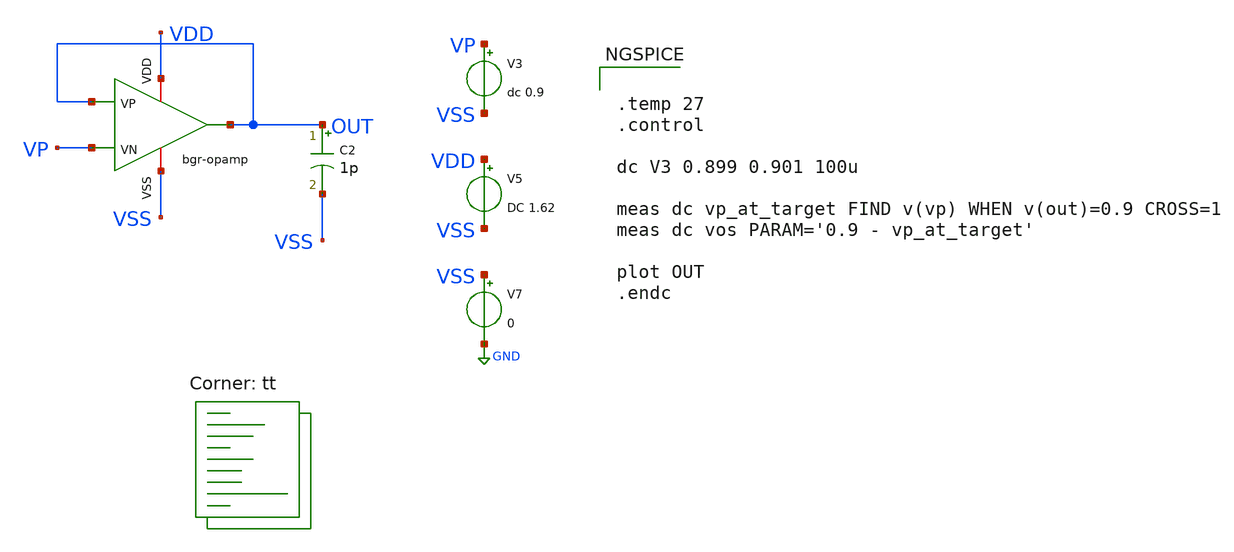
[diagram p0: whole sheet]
** sch_path: bandgap/bgr-opamp/tb_dc.sch
**.subckt tb_dc
V3 VP VSS dc 0.9
V5 VDD VSS DC 1.62
V7 VSS GND 0
C2 OUT VSS 1p m=1
x1 VDD OUT OUT VP VSS bgr-opamp
**** begin user architecture code


.temp 27
.control

dc V3 0.899 0.901 100u

meas dc vp_at_target FIND v(vp) WHEN v(out)=0.9 CROSS=1
meas dc vos PARAM='0.9 - vp_at_target'

plot OUT
.endc


.lib $::SKYWATER_MODELS/sky130.lib.spice tt
**** end user architecture code
**.ends

* expanding   symbol:  afe-icdec-teknofest-2026/bandgap/bgr-opamp/bgr-opamp.sym # of pins=5
** sym_path: bandgap/bgr-opamp/bgr-opamp.sym
** sch_path: bandgap/bgr-opamp/bgr-opamp.sch
.subckt bgr-opamp VDD OUT VP VN VSS
*.iopin VSS
*.iopin VDD
*.ipin VP
*.ipin VN
*.opin OUT
XM2 net2 VN net3 VSS sky130_fd_pr__nfet_01v8 L=0.3 W=30 nf=2 ad='int((nf+1)/2) * W/nf * 0.29' as='int((nf+2)/2) * W/nf * 0.29'
+ pd='2*int((nf+1)/2) * (W/nf + 0.29)' ps='2*int((nf+2)/2) * (W/nf + 0.29)' nrd='0.29 / W' nrs='0.29 / W'
+ sa=0 sb=0 sd=0 mult=1 m=1
XM4 net2 net1 VDD VDD sky130_fd_pr__pfet_01v8 L=1.25 W=10.8 nf=4 ad='int((nf+1)/2) * W/nf * 0.29' as='int((nf+2)/2) * W/nf * 0.29'
+ pd='2*int((nf+1)/2) * (W/nf + 0.29)' ps='2*int((nf+2)/2) * (W/nf + 0.29)' nrd='0.29 / W' nrs='0.29 / W'
+ sa=0 sb=0 sd=0 mult=1 m=1
XM3 net1 net1 VDD VDD sky130_fd_pr__pfet_01v8 L=1.25 W=10.8 nf=4 ad='int((nf+1)/2) * W/nf * 0.29' as='int((nf+2)/2) * W/nf * 0.29'
+ pd='2*int((nf+1)/2) * (W/nf + 0.29)' ps='2*int((nf+2)/2) * (W/nf + 0.29)' nrd='0.29 / W' nrs='0.29 / W'
+ sa=0 sb=0 sd=0 mult=1 m=1
XM5 net3 net11 VSS VSS sky130_fd_pr__nfet_01v8 L=1.25 W=3.4 nf=1 ad='int((nf+1)/2) * W/nf * 0.29' as='int((nf+2)/2) * W/nf * 0.29'
+ pd='2*int((nf+1)/2) * (W/nf + 0.29)' ps='2*int((nf+2)/2) * (W/nf + 0.29)' nrd='0.29 / W' nrs='0.29 / W'
+ sa=0 sb=0 sd=0 mult=1 m=1
XM9 net4 net5 net12 VSS sky130_fd_pr__nfet_01v8 L=1.25 W=13.6 nf=1 ad='int((nf+1)/2) * W/nf * 0.29' as='int((nf+2)/2) * W/nf * 0.29'
+ pd='2*int((nf+1)/2) * (W/nf + 0.29)' ps='2*int((nf+2)/2) * (W/nf + 0.29)' nrd='0.29 / W' nrs='0.29 / W'
+ sa=0 sb=0 sd=0 mult=1 m=1
XM8 net4 net4 VDD VDD sky130_fd_pr__pfet_01v8 L=1.25 W=10.8 nf=4 ad='int((nf+1)/2) * W/nf * 0.29' as='int((nf+2)/2) * W/nf * 0.29'
+ pd='2*int((nf+1)/2) * (W/nf + 0.29)' ps='2*int((nf+2)/2) * (W/nf + 0.29)' nrd='0.29 / W' nrs='0.29 / W'
+ sa=0 sb=0 sd=0 mult=1 m=1
XM11 net5 net4 VDD VDD sky130_fd_pr__pfet_01v8 L=1.25 W=10.8 nf=4 ad='int((nf+1)/2) * W/nf * 0.29' as='int((nf+2)/2) * W/nf * 0.29'
+ pd='2*int((nf+1)/2) * (W/nf + 0.29)' ps='2*int((nf+2)/2) * (W/nf + 0.29)' nrd='0.29 / W' nrs='0.29 / W'
+ sa=0 sb=0 sd=0 mult=1 m=1
XM10 net5 net5 net6 net6 sky130_fd_pr__nfet_01v8 L=1.25 W=3.4 nf=1 ad='int((nf+1)/2) * W/nf * 0.29' as='int((nf+2)/2) * W/nf * 0.29'
+ pd='2*int((nf+1)/2) * (W/nf + 0.29)' ps='2*int((nf+2)/2) * (W/nf + 0.29)' nrd='0.29 / W' nrs='0.29 / W'
+ sa=0 sb=0 sd=0 mult=1 m=1
XM6 OUT net2 VDD VDD sky130_fd_pr__pfet_01v8 L=1.25 W=100 nf=32 ad='int((nf+1)/2) * W/nf * 0.29' as='int((nf+2)/2) * W/nf * 0.29'
+ pd='2*int((nf+1)/2) * (W/nf + 0.29)' ps='2*int((nf+2)/2) * (W/nf + 0.29)' nrd='0.29 / W' nrs='0.29 / W'
+ sa=0 sb=0 sd=0 mult=1 m=1
XM7 OUT net11 VSS VSS sky130_fd_pr__nfet_01v8 L=1.25 W=14 nf=4 ad='int((nf+1)/2) * W/nf * 0.29' as='int((nf+2)/2) * W/nf * 0.29'
+ pd='2*int((nf+1)/2) * (W/nf + 0.29)' ps='2*int((nf+2)/2) * (W/nf + 0.29)' nrd='0.29 / W' nrs='0.29 / W'
+ sa=0 sb=0 sd=0 mult=1 m=1
XC2 OUT net2 sky130_fd_pr__cap_mim_m3_1 W=25 L=25 MF=32 m=32
XR2 net7 net12 VSS sky130_fd_pr__res_high_po_1p41 L=3.235 mult=1 m=1
XR3 net9 net7 VSS sky130_fd_pr__res_high_po_1p41 L=3.235 mult=1 m=1
XR4 net8 net9 VSS sky130_fd_pr__res_high_po_1p41 L=3.235 mult=1 m=1
XR5 net10 net8 VSS sky130_fd_pr__res_high_po_1p41 L=3.235 mult=1 m=1
XR6 VSS net10 VSS sky130_fd_pr__res_high_po_1p41 L=3.235 mult=1 m=1
XM13 net11 net4 VDD VDD sky130_fd_pr__pfet_01v8 L=1.25 W=10.8 nf=4 ad='int((nf+1)/2) * W/nf * 0.29' as='int((nf+2)/2) * W/nf * 0.29'
+ pd='2*int((nf+1)/2) * (W/nf + 0.29)' ps='2*int((nf+2)/2) * (W/nf + 0.29)' nrd='0.29 / W' nrs='0.29 / W'
+ sa=0 sb=0 sd=0 mult=1 m=1
XM14 net11 net11 VSS VSS sky130_fd_pr__nfet_01v8 L=1.25 W=6.8 nf=1 ad='int((nf+1)/2) * W/nf * 0.29' as='int((nf+2)/2) * W/nf * 0.29'
+ pd='2*int((nf+1)/2) * (W/nf + 0.29)' ps='2*int((nf+2)/2) * (W/nf + 0.29)' nrd='0.29 / W' nrs='0.29 / W'
+ sa=0 sb=0 sd=0 mult=1 m=1
XM15 net6 net6 VSS VSS sky130_fd_pr__nfet_01v8 L=1.25 W=3.4 nf=1 ad='int((nf+1)/2) * W/nf * 0.29' as='int((nf+2)/2) * W/nf * 0.29'
+ pd='2*int((nf+1)/2) * (W/nf + 0.29)' ps='2*int((nf+2)/2) * (W/nf + 0.29)' nrd='0.29 / W' nrs='0.29 / W'
+ sa=0 sb=0 sd=0 mult=1 m=1
XM12 net5 net4 net4 VSS sky130_fd_pr__pfet_01v8 L=0.15 W=0.85 nf=1 ad='int((nf+1)/2) * W/nf * 0.29' as='int((nf+2)/2) * W/nf * 0.29'
+ pd='2*int((nf+1)/2) * (W/nf + 0.29)' ps='2*int((nf+2)/2) * (W/nf + 0.29)' nrd='0.29 / W' nrs='0.29 / W'
+ sa=0 sb=0 sd=0 mult=1 m=1
XM16 net1 VP net3 VSS sky130_fd_pr__nfet_01v8 L=0.3 W=30 nf=2 ad='int((nf+1)/2) * W/nf * 0.29' as='int((nf+2)/2) * W/nf * 0.29'
+ pd='2*int((nf+1)/2) * (W/nf + 0.29)' ps='2*int((nf+2)/2) * (W/nf + 0.29)' nrd='0.29 / W' nrs='0.29 / W'
+ sa=0 sb=0 sd=0 mult=1 m=1
.ends

.GLOBAL GND
.end
